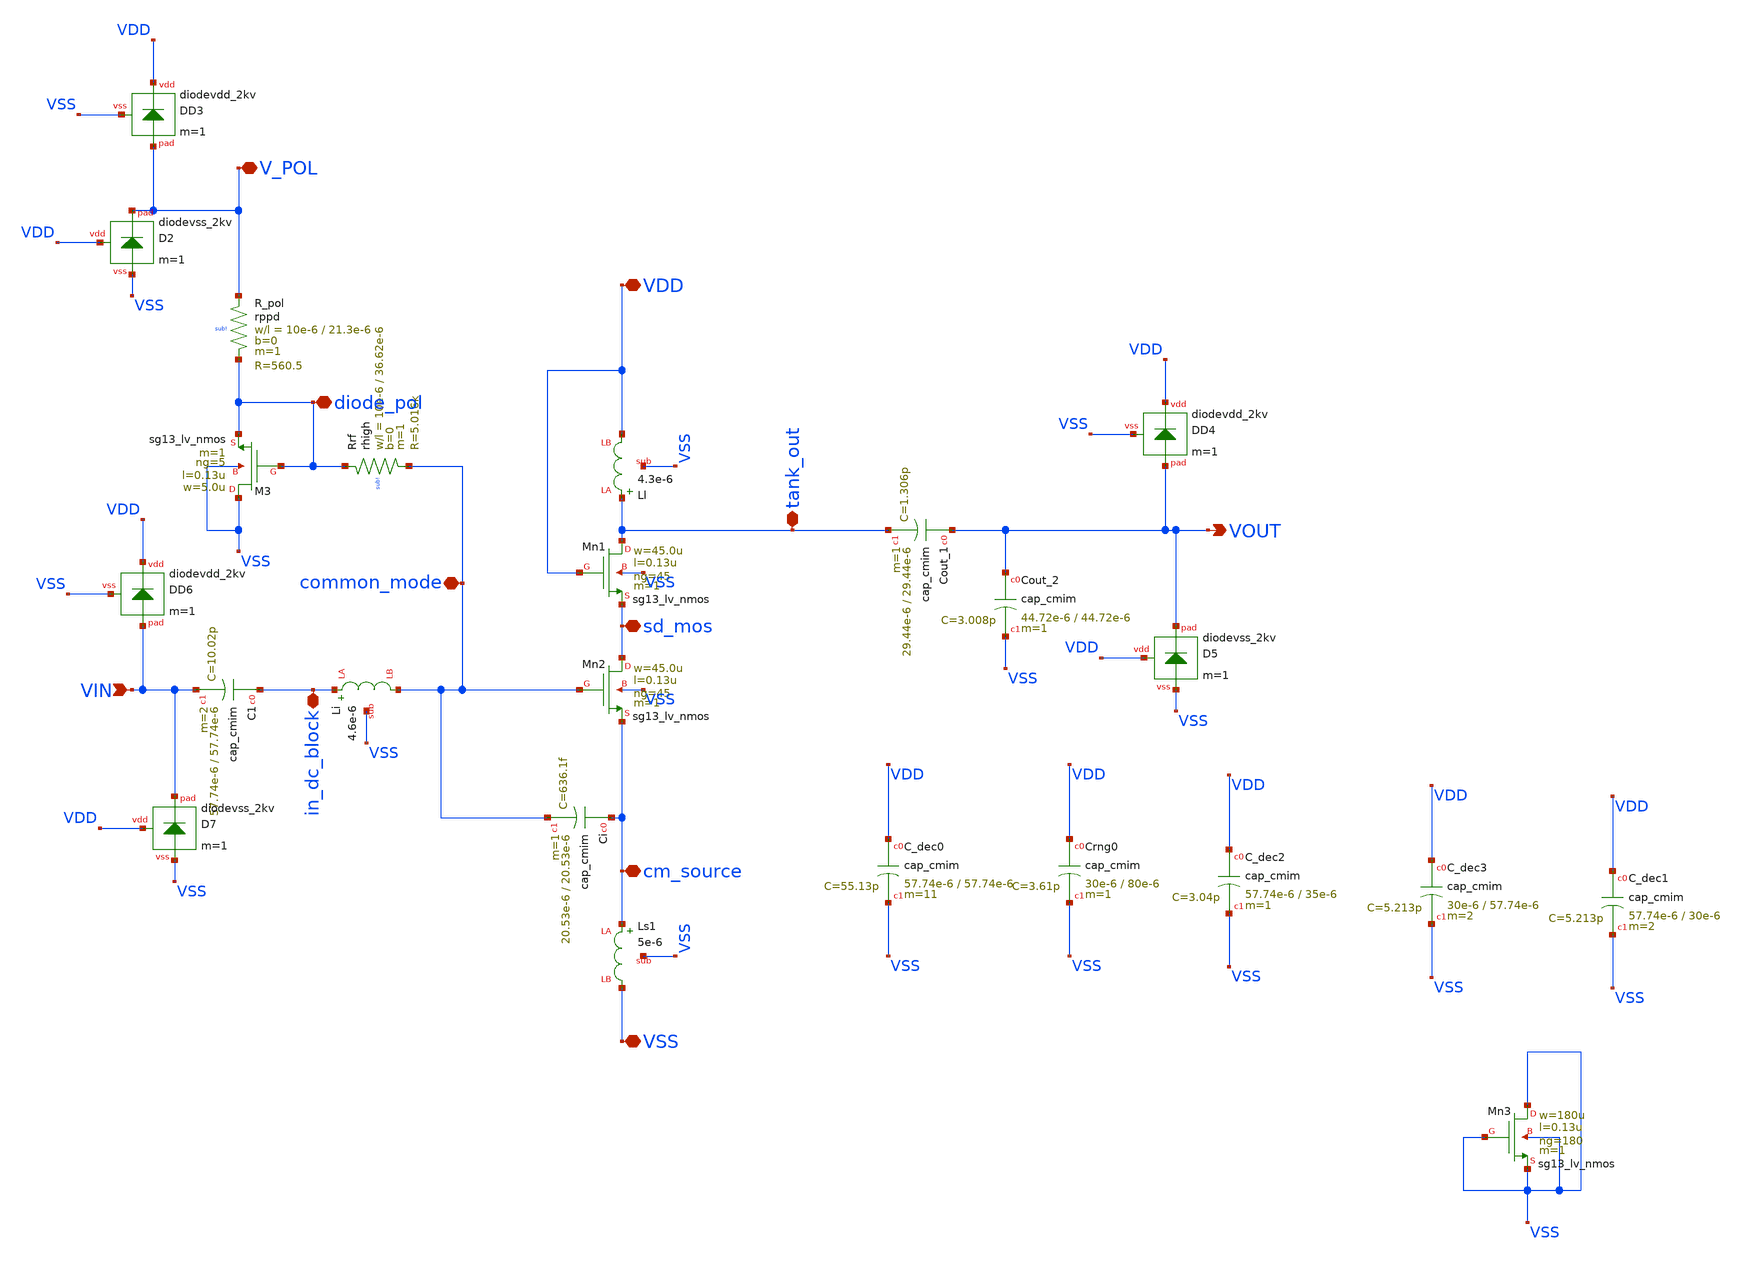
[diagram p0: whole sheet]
** sch_path: LNA_2.45G/design_data/xschem/circuit_lvs.sch
**.subckt circuit_lvs VOUT VIN VSS VDD V_POL diode_pol common_mode in_dc_block cm_source sd_mos
*+ tank_out
*.opin VOUT
*.ipin VIN
*.iopin VSS
*.iopin VDD
*.iopin V_POL
*.iopin diode_pol
*.iopin common_mode
*.iopin in_dc_block
*.iopin cm_source
*.iopin sd_mos
*.iopin tank_out
CC1 in_dc_block VIN cap_cmim w=57.74e-6 l=57.74e-6 m=2 mm_ok=1
MMn2 sd_mos common_mode cm_source VSS sg13_lv_nmos w=45.0u l=0.13u ng=45 m=1 mm_ok=1
CCi cm_source common_mode cap_cmim w=20.53e-6 l=20.53e-6 m=1 mm_ok=1
MMn1 tank_out VDD sd_mos VSS sg13_lv_nmos w=45.0u l=0.13u ng=45 m=1 mm_ok=1
MM3 VSS diode_pol diode_pol VSS sg13_lv_nmos w=5.0u l=0.13u ng=5 m=1 mm_ok=1
RRrf diode_pol common_mode sub! rhigh w=10e-6 l=36.62e-6 m=1 b=0 mm_ok=1
RR_pol V_POL diode_pol sub! rppd w=10e-6 l=21.3e-6 m=1 b=0 mm_ok=1
CCout_1 VOUT tank_out cap_cmim w=29.44e-6 l=29.44e-6 m=1 mm_ok=1
CCout_2 VOUT VSS cap_cmim w=44.72e-6 l=44.72e-6 m=1 mm_ok=1
CC_dec0 VDD VSS cap_cmim w=57.74e-6 l=57.74e-6 m=11 mm_ok=1
CC_dec1 VDD VSS cap_cmim w=57.74e-6 l=30e-6 m=2 mm_ok=1
CC_dec2 VDD VSS cap_cmim w=57.74e-6 l=35e-6 m=1 mm_ok=1
CC_dec3 VDD VSS cap_cmim w=30e-6 l=57.74e-6 m=2 mm_ok=1
CCrng0 VDD VSS cap_cmim w=30e-6 l=80e-6 m=1 mm_ok=1
MMn3 VSS VSS VSS VSS sg13_lv_nmos w=180u l=0.13u ng=180 m=1 mm_ok=1
LLi in_dc_block common_mode VSS simple_inductor w=4.6e-6 s=4.1e-6 d=167.7e-6 nr_r=1
LLl tank_out VDD VSS simple_inductor w=4.3e-6 s=4e-6 d=176.3e-6 nr_r=1
LLs1 cm_source VSS VSS simple_inductor w=5e-6 s=2.1e-6 d=113.2e-6 nr_r=1
DD2 VDD V_POL VSS diodevss_2kv m=1
DD3 VDD V_POL VSS diodevdd_2kv m=1
DD4 VDD VOUT VSS diodevdd_2kv m=1
DD5 VDD VOUT VSS diodevss_2kv m=1
DD6 VDD VIN VSS diodevdd_2kv m=1
DD7 VDD VIN VSS diodevss_2kv m=1
**.ends
.end
